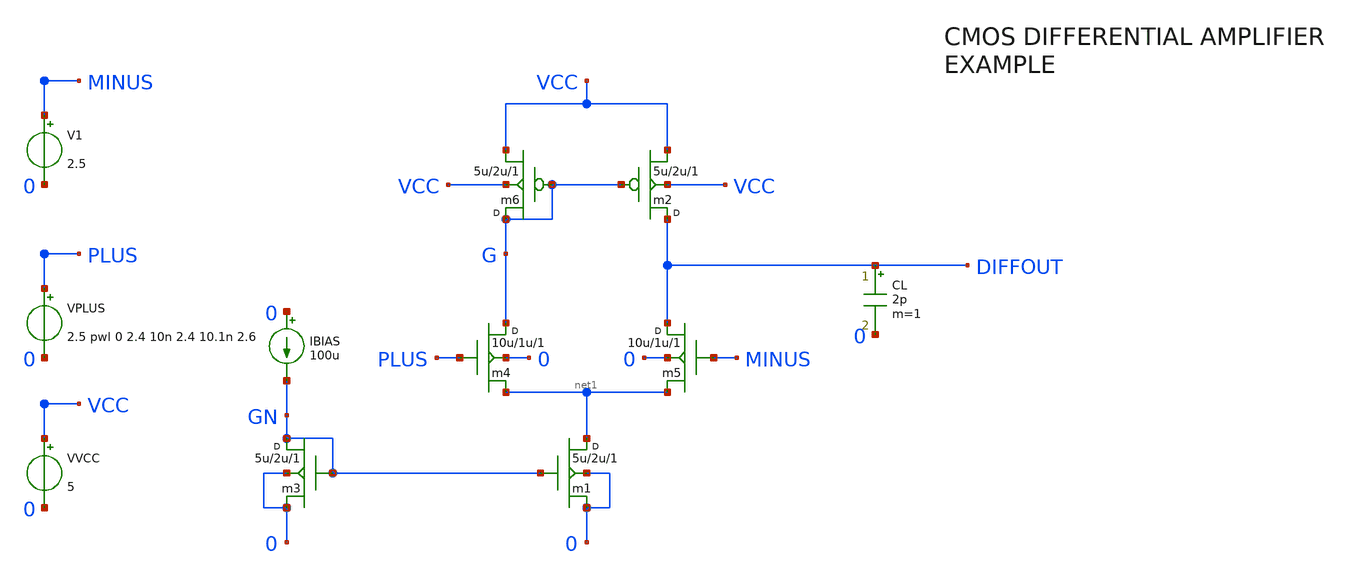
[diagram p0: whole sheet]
** sch_path: xschem_library/examples/cmos_example.sch
**.subckt cmos_example
m1 net1 GN 0 0 cmosn w=5u l=2u m=1
m2 DIFFOUT G VCC VCC cmosp w=5u l=2u m=1
VVCC VCC 0 5
m3 GN GN 0 0 cmosn w=5u l=2u m=1
IBIAS 0 GN 100u
m4 G PLUS net1 0 cmosn w=10u l=1u m=1
m5 DIFFOUT MINUS net1 0 cmosn w=10u l=1u m=1
m6 G G VCC VCC cmosp w=5u l=2u m=1
VPLUS PLUS 0 2.5 pwl 0 2.4 10n 2.4 10.1n 2.6
V1 MINUS 0 2.5
CL DIFFOUT 0 2p m=1
**** begin user architecture code


** ngspice
.temp 30

** xyce
* .step temp list 30

** ngspice
* .save all

** models are generally not free: you must download
** SPICE models for active devices and put them  into the below
** referenced file in netlist/simulation directory.
.option savecurrents
.include "models_cmos_example.txt"
.control
let cap = 2e-12
set filetype=binary
while cap <= 20e-12
alter CL cap
tran 0.8n 2000n
write cmos_example.raw
set appendwrite
let cap = cap + 2e-12
end
* op
write cmos_example.raw
plot all.diffout
.endc

** ngspice
* .save all

** xyce, not needed if -r given om cmdline
* .print tran format=raw v(diffout) v(plus) v(minus)


**** end user architecture code
**.ends
.end
